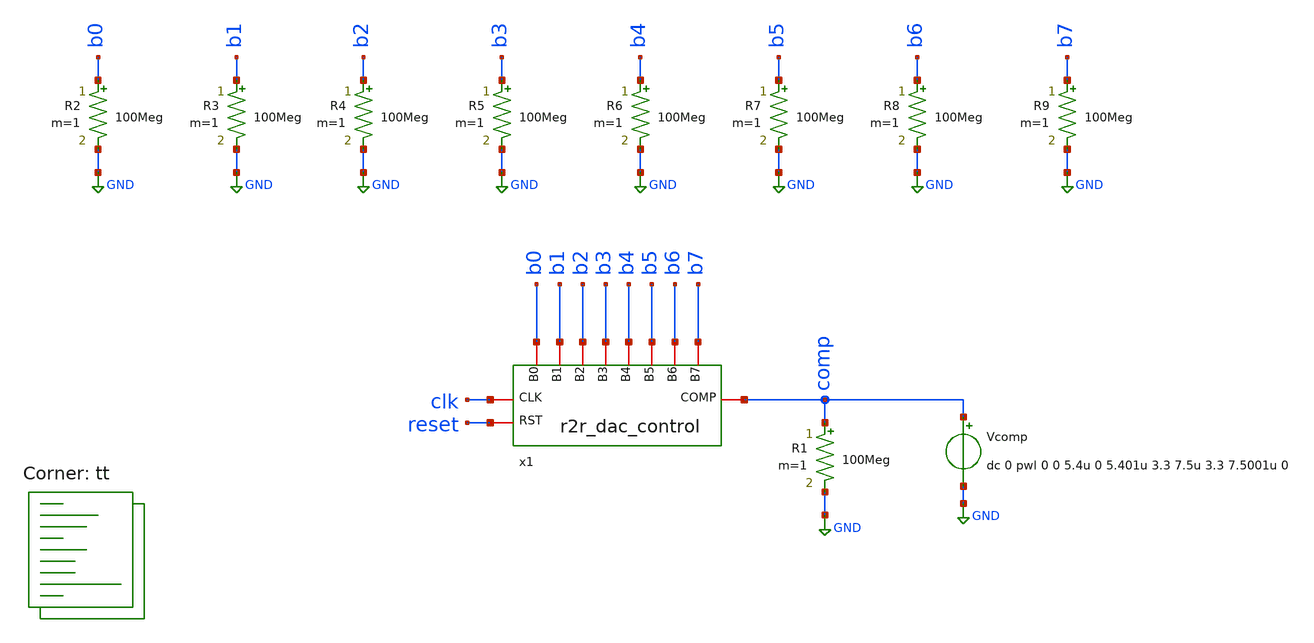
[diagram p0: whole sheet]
** sch_path: xschem/tb_dac_control.sch
**.subckt tb_dac_control
x1 reset clk comp b7 b6 b5 b4 b3 b2 b1 b0 r2r_dac_control
R1 comp GND 100Meg m=1
R2 b0 GND 100Meg m=1
R3 b1 GND 100Meg m=1
R4 b2 GND 100Meg m=1
R5 b3 GND 100Meg m=1
R6 b4 GND 100Meg m=1
R7 b5 GND 100Meg m=1
R8 b6 GND 100Meg m=1
R9 b7 GND 100Meg m=1
Vcomp comp GND dc 0 pwl 0 0 5.4u 0 5.401u 3.3 7.5u 3.3 7.5001u 0
**** begin user architecture code
.lib $::SKYWATER_MODELS/sky130.lib.spice tt



.option chgtol=4e-16

*.param TEMPGAUSS = agauss(30, 40, 1)
*.option temp = 'TEMPGAUSS'
*.param DELTA = 0.002

* .param vdda 3.3
.option TNOM=27 GMIN=1e-15 reltol=1e-3 method=gear
.param TRF = 10p
.param AVDD = 3.3
.param PERIOD_CLK = 1u
.param PW_CLK = PERIOD_CLK/2



* VCLK clk 0 dc 0 pulse (0 3.3 0 10p 10p 500n 1u)
VCLK clk 0 dc 0 pulse (0 {AVDD} 0 {TRF} {TRF} {PW_CLK} {PERIOD_CLK})
VRESET reset 0 dc {AVDD} pwl 0 {AVDD} {PW_CLK*4} {AVDD} {PW_CLK*2 + 1n} 0


.control
set num_threads=8
unset askquit

*optran 0 0 0 1n 1u 0

*- Override the default digital output bridge.
pre_set auto_bridge_d_out =
     + ( ".model auto_dac dac_bridge(out_low = 0.0 out_high = 1.8)"
     +   "auto_bridge%d [ %s ] [ %s ] auto_dac" )



   setseed 3
   *reset
   save all
   tran 100p 15u
   write tb_dac_control.raw
   *reset
   set appendwrite
.endc






*.include ./../cosim/r2r_dac_control.spice

.subckt r2r_dac_control reset clk comp b7 b6 b5 b4 b3 b2 b1 b0

adut [clk  reset  comp  ]  [b7  b6  b5  b4  b3  b2  b1  b0  ] null r2r_ctrl

.model r2r_ctrl d_cosim
+ simulation="/home/ttuser/tinytapeout/TT_Project/verilog/sim/r2r_dac_control.so" delay=10p
.ends r2r_dac_control


**** end user architecture code
**.ends
.GLOBAL GND
.end
